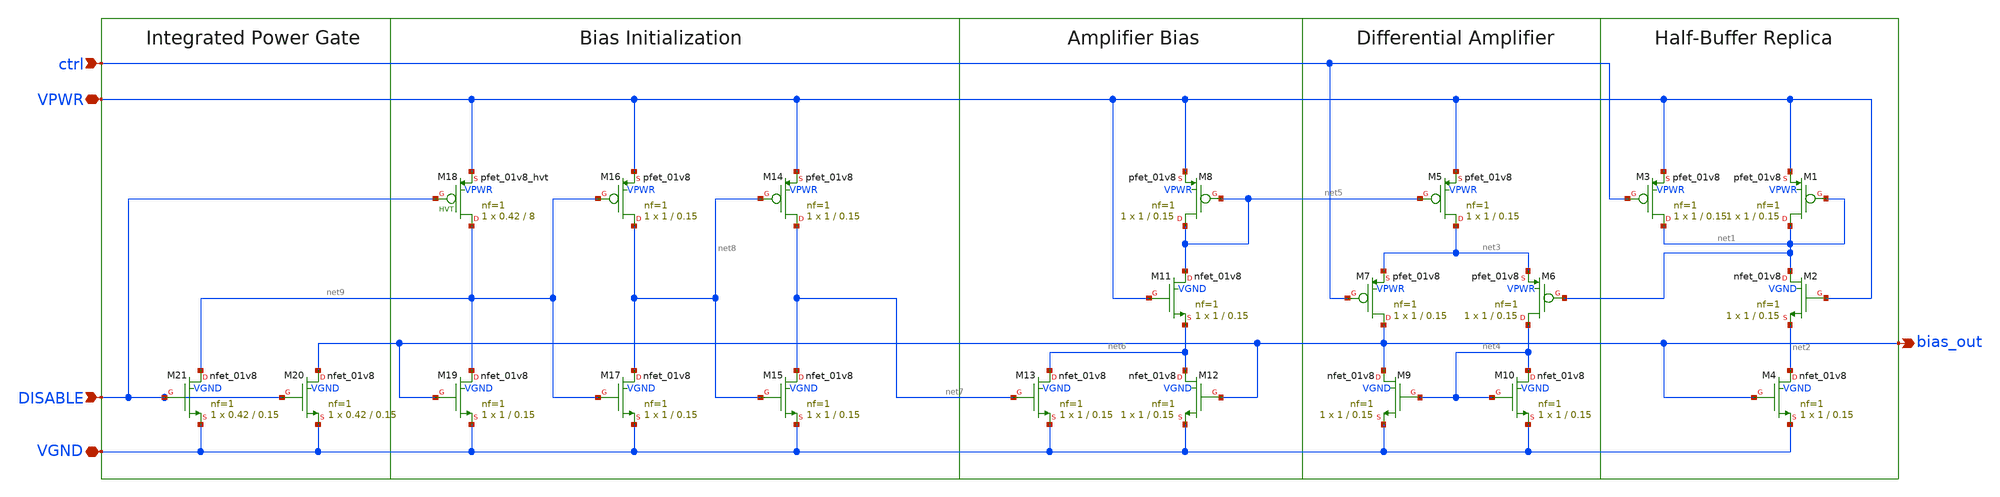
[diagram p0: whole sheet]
** sch_path: simple_vco/v1/bias_gen.sch
**.subckt bias_gen VPWR VGND DISABLE ctrl bias_out
*.iopin VPWR
*.iopin VGND
*.ipin DISABLE
*.ipin ctrl
*.opin bias_out
XM8 net5 net5 VPWR VPWR sky130_fd_pr__pfet_01v8 L=0.15 W=1 nf=1 ad='int((1 + 1)/2) * 1 / 1 * 0.29' as='int((1 + 2)/2) * 1 / 1 * 0.29'
+ pd='2*int((1 + 1)/2) * (1 / 1 + 0.29)' ps='2*int((1 + 2)/2) * (1 / 1 + 0.29)' nrd='0.29 / 1 ' nrs='0.29 / 1 '
+ sa=0 sb=0 sd=0 mult=1 m=1
XM7 bias_out ctrl net3 VPWR sky130_fd_pr__pfet_01v8 L=0.15 W=1 nf=1 ad='int((1 + 1)/2) * 1 / 1 * 0.29'
+ as='int((1 + 2)/2) * 1 / 1 * 0.29' pd='2*int((1 + 1)/2) * (1 / 1 + 0.29)' ps='2*int((1 + 2)/2) * (1 / 1 + 0.29)'
+ nrd='0.29 / 1 ' nrs='0.29 / 1 ' sa=0 sb=0 sd=0 mult=1 m=1
XM6 net4 net1 net3 VPWR sky130_fd_pr__pfet_01v8 L=0.15 W=1 nf=1 ad='int((1 + 1)/2) * 1 / 1 * 0.29' as='int((1 + 2)/2) * 1 / 1 * 0.29'
+ pd='2*int((1 + 1)/2) * (1 / 1 + 0.29)' ps='2*int((1 + 2)/2) * (1 / 1 + 0.29)' nrd='0.29 / 1 ' nrs='0.29 / 1 '
+ sa=0 sb=0 sd=0 mult=1 m=1
XM3 net1 ctrl VPWR VPWR sky130_fd_pr__pfet_01v8 L=0.15 W=1 nf=1 ad='int((1 + 1)/2) * 1 / 1 * 0.29' as='int((1 + 2)/2) * 1 / 1 * 0.29'
+ pd='2*int((1 + 1)/2) * (1 / 1 + 0.29)' ps='2*int((1 + 2)/2) * (1 / 1 + 0.29)' nrd='0.29 / 1 ' nrs='0.29 / 1 '
+ sa=0 sb=0 sd=0 mult=1 m=1
XM1 net1 net1 VPWR VPWR sky130_fd_pr__pfet_01v8 L=0.15 W=1 nf=1 ad='int((1 + 1)/2) * 1 / 1 * 0.29' as='int((1 + 2)/2) * 1 / 1 * 0.29'
+ pd='2*int((1 + 1)/2) * (1 / 1 + 0.29)' ps='2*int((1 + 2)/2) * (1 / 1 + 0.29)' nrd='0.29 / 1 ' nrs='0.29 / 1 '
+ sa=0 sb=0 sd=0 mult=1 m=1
XM5 net3 net5 VPWR VPWR sky130_fd_pr__pfet_01v8 L=0.15 W=1 nf=1 ad='int((1 + 1)/2) * 1 / 1 * 0.29' as='int((1 + 2)/2) * 1 / 1 * 0.29'
+ pd='2*int((1 + 1)/2) * (1 / 1 + 0.29)' ps='2*int((1 + 2)/2) * (1 / 1 + 0.29)' nrd='0.29 / 1 ' nrs='0.29 / 1 '
+ sa=0 sb=0 sd=0 mult=1 m=1
XM9 bias_out net4 VGND VGND sky130_fd_pr__nfet_01v8 L=0.15 W=1 nf=1 ad='int((1 + 1)/2) * 1 / 1 * 0.29'
+ as='int((1 + 2)/2) * 1 / 1 * 0.29' pd='2*int((1 + 1)/2) * (1 / 1 + 0.29)' ps='2*int((1 + 2)/2) * (1 / 1 + 0.29)'
+ nrd='0.29 / 1 ' nrs='0.29 / 1 ' sa=0 sb=0 sd=0 mult=1 m=1
XM10 net4 net4 VGND VGND sky130_fd_pr__nfet_01v8 L=0.15 W=1 nf=1 ad='int((1 + 1)/2) * 1 / 1 * 0.29' as='int((1 + 2)/2) * 1 / 1 * 0.29'
+ pd='2*int((1 + 1)/2) * (1 / 1 + 0.29)' ps='2*int((1 + 2)/2) * (1 / 1 + 0.29)' nrd='0.29 / 1 ' nrs='0.29 / 1 '
+ sa=0 sb=0 sd=0 mult=1 m=1
XM11 net5 VPWR net6 VGND sky130_fd_pr__nfet_01v8 L=0.15 W=1 nf=1 ad='int((1 + 1)/2) * 1 / 1 * 0.29' as='int((1 + 2)/2) * 1 / 1 * 0.29'
+ pd='2*int((1 + 1)/2) * (1 / 1 + 0.29)' ps='2*int((1 + 2)/2) * (1 / 1 + 0.29)' nrd='0.29 / 1 ' nrs='0.29 / 1 '
+ sa=0 sb=0 sd=0 mult=1 m=1
XM12 net6 bias_out VGND VGND sky130_fd_pr__nfet_01v8 L=0.15 W=1 nf=1 ad='int((1 + 1)/2) * 1 / 1 * 0.29'
+ as='int((1 + 2)/2) * 1 / 1 * 0.29' pd='2*int((1 + 1)/2) * (1 / 1 + 0.29)' ps='2*int((1 + 2)/2) * (1 / 1 + 0.29)'
+ nrd='0.29 / 1 ' nrs='0.29 / 1 ' sa=0 sb=0 sd=0 mult=1 m=1
XM13 net6 net7 VGND VGND sky130_fd_pr__nfet_01v8 L=0.15 W=1 nf=1 ad='int((1 + 1)/2) * 1 / 1 * 0.29' as='int((1 + 2)/2) * 1 / 1 * 0.29'
+ pd='2*int((1 + 1)/2) * (1 / 1 + 0.29)' ps='2*int((1 + 2)/2) * (1 / 1 + 0.29)' nrd='0.29 / 1 ' nrs='0.29 / 1 '
+ sa=0 sb=0 sd=0 mult=1 m=1
XM14 net7 net8 VPWR VPWR sky130_fd_pr__pfet_01v8 L=0.15 W=1 nf=1 ad='int((1 + 1)/2) * 1 / 1 * 0.29' as='int((1 + 2)/2) * 1 / 1 * 0.29'
+ pd='2*int((1 + 1)/2) * (1 / 1 + 0.29)' ps='2*int((1 + 2)/2) * (1 / 1 + 0.29)' nrd='0.29 / 1 ' nrs='0.29 / 1 '
+ sa=0 sb=0 sd=0 mult=1 m=1
XM15 net7 net8 VGND VGND sky130_fd_pr__nfet_01v8 L=0.15 W=1 nf=1 ad='int((1 + 1)/2) * 1 / 1 * 0.29' as='int((1 + 2)/2) * 1 / 1 * 0.29'
+ pd='2*int((1 + 1)/2) * (1 / 1 + 0.29)' ps='2*int((1 + 2)/2) * (1 / 1 + 0.29)' nrd='0.29 / 1 ' nrs='0.29 / 1 '
+ sa=0 sb=0 sd=0 mult=1 m=1
XM16 net8 net9 VPWR VPWR sky130_fd_pr__pfet_01v8 L=0.15 W=1 nf=1 ad='int((1 + 1)/2) * 1 / 1 * 0.29' as='int((1 + 2)/2) * 1 / 1 * 0.29'
+ pd='2*int((1 + 1)/2) * (1 / 1 + 0.29)' ps='2*int((1 + 2)/2) * (1 / 1 + 0.29)' nrd='0.29 / 1 ' nrs='0.29 / 1 '
+ sa=0 sb=0 sd=0 mult=1 m=1
XM17 net8 net9 VGND VGND sky130_fd_pr__nfet_01v8 L=0.15 W=1 nf=1 ad='int((1 + 1)/2) * 1 / 1 * 0.29' as='int((1 + 2)/2) * 1 / 1 * 0.29'
+ pd='2*int((1 + 1)/2) * (1 / 1 + 0.29)' ps='2*int((1 + 2)/2) * (1 / 1 + 0.29)' nrd='0.29 / 1 ' nrs='0.29 / 1 '
+ sa=0 sb=0 sd=0 mult=1 m=1
XM19 net9 bias_out VGND VGND sky130_fd_pr__nfet_01v8 L=0.15 W=1 nf=1 ad='int((1 + 1)/2) * 1 / 1 * 0.29'
+ as='int((1 + 2)/2) * 1 / 1 * 0.29' pd='2*int((1 + 1)/2) * (1 / 1 + 0.29)' ps='2*int((1 + 2)/2) * (1 / 1 + 0.29)'
+ nrd='0.29 / 1 ' nrs='0.29 / 1 ' sa=0 sb=0 sd=0 mult=1 m=1
XM18 net9 DISABLE VPWR VPWR sky130_fd_pr__pfet_01v8_hvt L=8 W=0.42 nf=1 ad='int((1 + 1)/2) * 0.42 / 1 * 0.29'
+ as='int((1 + 2)/2) * 0.42 / 1 * 0.29' pd='2*int((1 + 1)/2) * (0.42 / 1 + 0.29)' ps='2*int((1 + 2)/2) * (0.42 / 1 + 0.29)'
+ nrd='0.29 / 0.42 ' nrs='0.29 / 0.42 ' sa=0 sb=0 sd=0 mult=1 m=1
XM20 bias_out DISABLE VGND VGND sky130_fd_pr__nfet_01v8 L=0.15 W=0.42 nf=1 ad='int((1 + 1)/2) * 0.42 / 1 * 0.29'
+ as='int((1 + 2)/2) * 0.42 / 1 * 0.29' pd='2*int((1 + 1)/2) * (0.42 / 1 + 0.29)' ps='2*int((1 + 2)/2) * (0.42 / 1 + 0.29)'
+ nrd='0.29 / 0.42 ' nrs='0.29 / 0.42 ' sa=0 sb=0 sd=0 mult=1 m=1
XM21 net9 DISABLE VGND VGND sky130_fd_pr__nfet_01v8 L=0.15 W=0.42 nf=1 ad='int((1 + 1)/2) * 0.42 / 1 * 0.29'
+ as='int((1 + 2)/2) * 0.42 / 1 * 0.29' pd='2*int((1 + 1)/2) * (0.42 / 1 + 0.29)' ps='2*int((1 + 2)/2) * (0.42 / 1 + 0.29)'
+ nrd='0.29 / 0.42 ' nrs='0.29 / 0.42 ' sa=0 sb=0 sd=0 mult=1 m=1
XM4 net2 bias_out VGND VGND sky130_fd_pr__nfet_01v8 L=0.15 W=1 nf=1 ad='int((1 + 1)/2) * 1 / 1 * 0.29'
+ as='int((1 + 2)/2) * 1 / 1 * 0.29' pd='2*int((1 + 1)/2) * (1 / 1 + 0.29)' ps='2*int((1 + 2)/2) * (1 / 1 + 0.29)'
+ nrd='0.29 / 1 ' nrs='0.29 / 1 ' sa=0 sb=0 sd=0 mult=1 m=1
XM2 net1 VPWR net2 VGND sky130_fd_pr__nfet_01v8 L=0.15 W=1 nf=1 ad='int((1 + 1)/2) * 1 / 1 * 0.29' as='int((1 + 2)/2) * 1 / 1 * 0.29'
+ pd='2*int((1 + 1)/2) * (1 / 1 + 0.29)' ps='2*int((1 + 2)/2) * (1 / 1 + 0.29)' nrd='0.29 / 1 ' nrs='0.29 / 1 '
+ sa=0 sb=0 sd=0 mult=1 m=1
**.ends
.end
